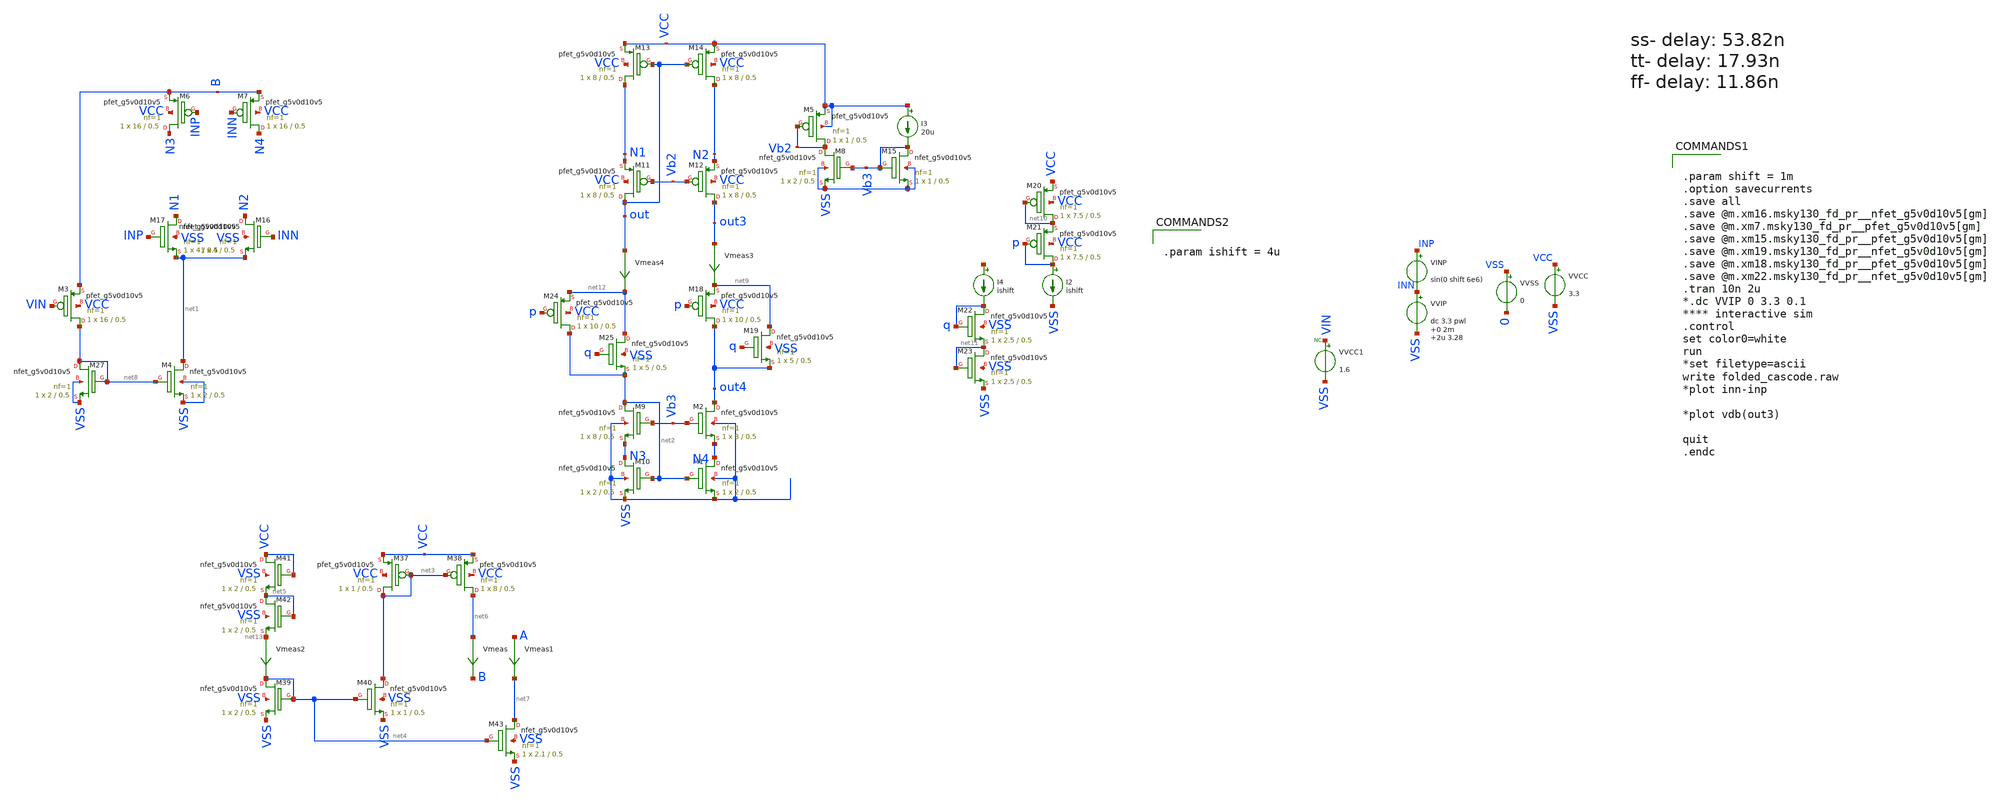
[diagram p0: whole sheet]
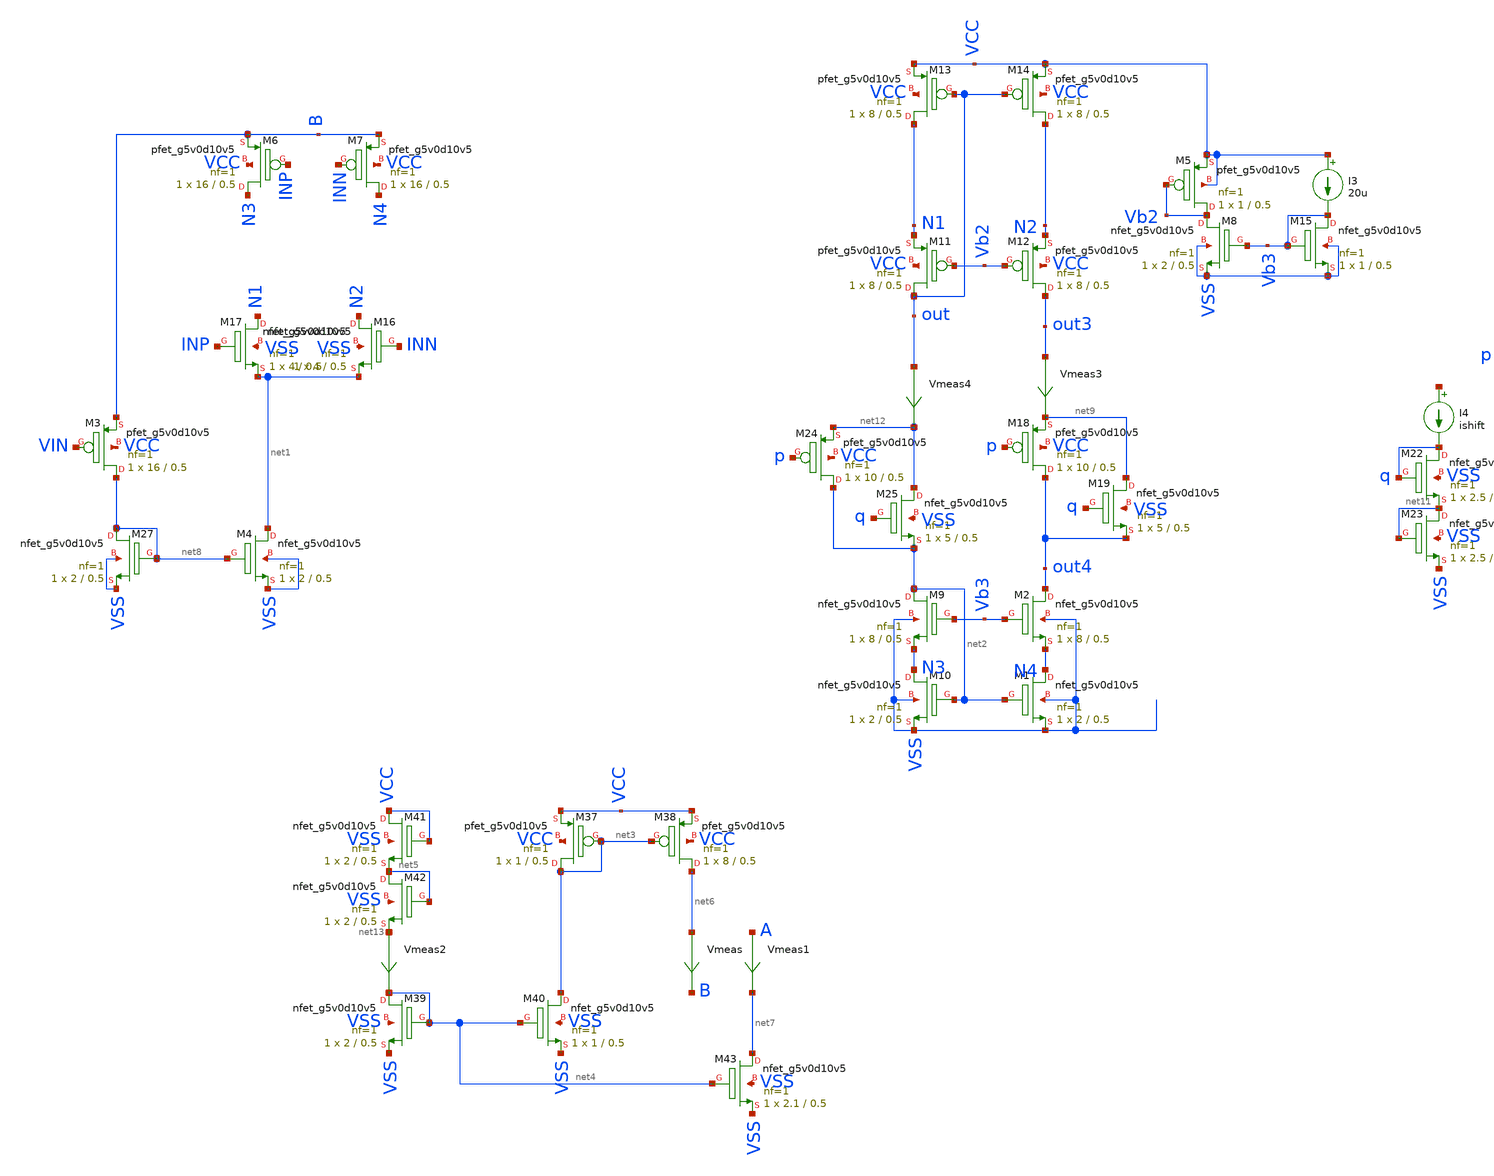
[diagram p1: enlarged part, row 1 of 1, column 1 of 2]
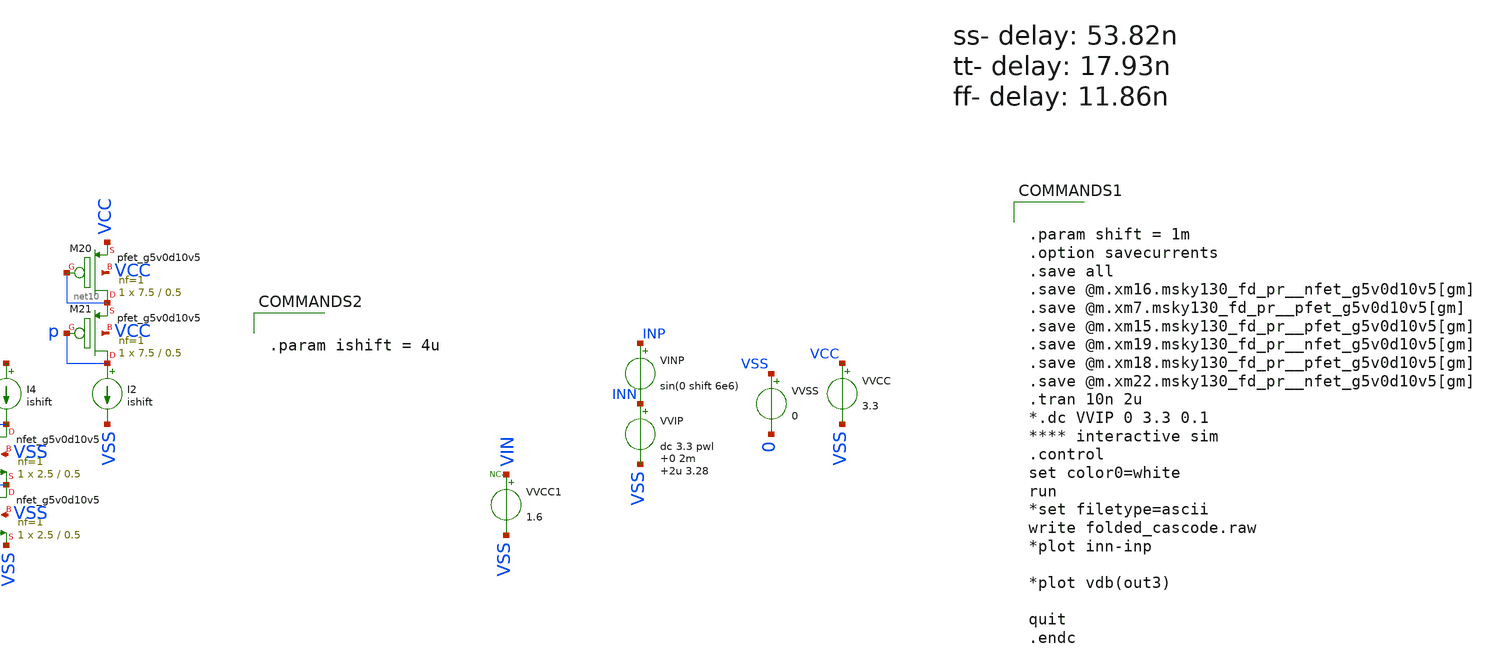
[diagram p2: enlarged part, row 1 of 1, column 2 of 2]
** sch_path: folded_cascode/folded_cascode_ab.sch
.lib $::SKYWATER_MODELS/sky130.lib.spice.tt.red tt
.include $::SKYWATER_STDCELLS/sky130_fd_sc_hd.spice

**.subckt folded_cascode_ab
XM1 N4 net2 VSS VSS sky130_fd_pr__nfet_g5v0d10v5 L=0.5 W=2 nf=1 ad='int((nf+1)/2) * W/nf * 0.29' as='int((nf+2)/2) * W/nf * 0.29'
+ pd='2*int((nf+1)/2) * (W/nf + 0.29)' ps='2*int((nf+2)/2) * (W/nf + 0.29)' nrd='0.29 / W' nrs='0.29 / W'
+ sa=0 sb=0 sd=0 mult=1 m=1
XM2 out4 Vb3 N4 VSS sky130_fd_pr__nfet_g5v0d10v5 L=0.5 W=8 nf=1 ad='int((nf+1)/2) * W/nf * 0.29' as='int((nf+2)/2) * W/nf * 0.29'
+ pd='2*int((nf+1)/2) * (W/nf + 0.29)' ps='2*int((nf+2)/2) * (W/nf + 0.29)' nrd='0.29 / W' nrs='0.29 / W'
+ sa=0 sb=0 sd=0 mult=1 m=1
XM9 net2 Vb3 N3 VSS sky130_fd_pr__nfet_g5v0d10v5 L=0.5 W=8 nf=1 ad='int((nf+1)/2) * W/nf * 0.29' as='int((nf+2)/2) * W/nf * 0.29'
+ pd='2*int((nf+1)/2) * (W/nf + 0.29)' ps='2*int((nf+2)/2) * (W/nf + 0.29)' nrd='0.29 / W' nrs='0.29 / W'
+ sa=0 sb=0 sd=0 mult=1 m=1
XM10 N3 net2 VSS VSS sky130_fd_pr__nfet_g5v0d10v5 L=0.5 W=2 nf=1 ad='int((nf+1)/2) * W/nf * 0.29' as='int((nf+2)/2) * W/nf * 0.29'
+ pd='2*int((nf+1)/2) * (W/nf + 0.29)' ps='2*int((nf+2)/2) * (W/nf + 0.29)' nrd='0.29 / W' nrs='0.29 / W'
+ sa=0 sb=0 sd=0 mult=1 m=1
XM11 out Vb2 N1 VCC sky130_fd_pr__pfet_g5v0d10v5 L=0.5 W=8 nf=1 ad='int((nf+1)/2) * W/nf * 0.29' as='int((nf+2)/2) * W/nf * 0.29'
+ pd='2*int((nf+1)/2) * (W/nf + 0.29)' ps='2*int((nf+2)/2) * (W/nf + 0.29)' nrd='0.29 / W' nrs='0.29 / W'
+ sa=0 sb=0 sd=0 mult=1 m=1
XM12 out3 Vb2 N2 VCC sky130_fd_pr__pfet_g5v0d10v5 L=0.5 W=8 nf=1 ad='int((nf+1)/2) * W/nf * 0.29' as='int((nf+2)/2) * W/nf * 0.29'
+ pd='2*int((nf+1)/2) * (W/nf + 0.29)' ps='2*int((nf+2)/2) * (W/nf + 0.29)' nrd='0.29 / W' nrs='0.29 / W'
+ sa=0 sb=0 sd=0 mult=1 m=1
XM13 N1 out VCC VCC sky130_fd_pr__pfet_g5v0d10v5 L=0.5 W=8 nf=1 ad='int((nf+1)/2) * W/nf * 0.29' as='int((nf+2)/2) * W/nf * 0.29'
+ pd='2*int((nf+1)/2) * (W/nf + 0.29)' ps='2*int((nf+2)/2) * (W/nf + 0.29)' nrd='0.29 / W' nrs='0.29 / W'
+ sa=0 sb=0 sd=0 mult=1 m=1
XM14 N2 out VCC VCC sky130_fd_pr__pfet_g5v0d10v5 L=0.5 W=8 nf=1 ad='int((nf+1)/2) * W/nf * 0.29' as='int((nf+2)/2) * W/nf * 0.29'
+ pd='2*int((nf+1)/2) * (W/nf + 0.29)' ps='2*int((nf+2)/2) * (W/nf + 0.29)' nrd='0.29 / W' nrs='0.29 / W'
+ sa=0 sb=0 sd=0 mult=1 m=1
XM16 N2 INN net1 VSS sky130_fd_pr__nfet_g5v0d10v5 L=0.5 W=4 nf=1 ad='int((nf+1)/2) * W/nf * 0.29' as='int((nf+2)/2) * W/nf * 0.29'
+ pd='2*int((nf+1)/2) * (W/nf + 0.29)' ps='2*int((nf+2)/2) * (W/nf + 0.29)' nrd='0.29 / W' nrs='0.29 / W'
+ sa=0 sb=0 sd=0 mult=1 m=1
XM17 N1 INP net1 VSS sky130_fd_pr__nfet_g5v0d10v5 L=0.5 W=4 nf=1 ad='int((nf+1)/2) * W/nf * 0.29' as='int((nf+2)/2) * W/nf * 0.29'
+ pd='2*int((nf+1)/2) * (W/nf + 0.29)' ps='2*int((nf+2)/2) * (W/nf + 0.29)' nrd='0.29 / W' nrs='0.29 / W'
+ sa=0 sb=0 sd=0 mult=1 m=1
XM6 N3 INP B VCC sky130_fd_pr__pfet_g5v0d10v5 L=0.5 W=16 nf=1 ad='int((nf+1)/2) * W/nf * 0.29' as='int((nf+2)/2) * W/nf * 0.29'
+ pd='2*int((nf+1)/2) * (W/nf + 0.29)' ps='2*int((nf+2)/2) * (W/nf + 0.29)' nrd='0.29 / W' nrs='0.29 / W'
+ sa=0 sb=0 sd=0 mult=1 m=1
XM7 N4 INN B VCC sky130_fd_pr__pfet_g5v0d10v5 L=0.5 W=16 nf=1 ad='int((nf+1)/2) * W/nf * 0.29' as='int((nf+2)/2) * W/nf * 0.29'
+ pd='2*int((nf+1)/2) * (W/nf + 0.29)' ps='2*int((nf+2)/2) * (W/nf + 0.29)' nrd='0.29 / W' nrs='0.29 / W'
+ sa=0 sb=0 sd=0 mult=1 m=1
XM37 net3 net3 VCC VCC sky130_fd_pr__pfet_g5v0d10v5 L=0.5 W=1 nf=1 ad='int((nf+1)/2) * W/nf * 0.29' as='int((nf+2)/2) * W/nf * 0.29'
+ pd='2*int((nf+1)/2) * (W/nf + 0.29)' ps='2*int((nf+2)/2) * (W/nf + 0.29)' nrd='0.29 / W' nrs='0.29 / W'
+ sa=0 sb=0 sd=0 mult=1 m=1
XM38 net6 net3 VCC VCC sky130_fd_pr__pfet_g5v0d10v5 L=0.5 W=8 nf=1 ad='int((nf+1)/2) * W/nf * 0.29' as='int((nf+2)/2) * W/nf * 0.29'
+ pd='2*int((nf+1)/2) * (W/nf + 0.29)' ps='2*int((nf+2)/2) * (W/nf + 0.29)' nrd='0.29 / W' nrs='0.29 / W'
+ sa=0 sb=0 sd=0 mult=1 m=1
Vmeas net6 B 0
.save i(vmeas)
XM39 net4 net4 VSS VSS sky130_fd_pr__nfet_g5v0d10v5 L=0.5 W=2 nf=1 ad='int((nf+1)/2) * W/nf * 0.29' as='int((nf+2)/2) * W/nf * 0.29'
+ pd='2*int((nf+1)/2) * (W/nf + 0.29)' ps='2*int((nf+2)/2) * (W/nf + 0.29)' nrd='0.29 / W' nrs='0.29 / W'
+ sa=0 sb=0 sd=0 mult=1 m=1
XM40 net3 net4 VSS VSS sky130_fd_pr__nfet_g5v0d10v5 L=0.5 W=1 nf=1 ad='int((nf+1)/2) * W/nf * 0.29' as='int((nf+2)/2) * W/nf * 0.29'
+ pd='2*int((nf+1)/2) * (W/nf + 0.29)' ps='2*int((nf+2)/2) * (W/nf + 0.29)' nrd='0.29 / W' nrs='0.29 / W'
+ sa=0 sb=0 sd=0 mult=1 m=1
Vmeas2 net13 net4 0
.save i(vmeas2)
XM41 VCC VCC net5 VSS sky130_fd_pr__nfet_g5v0d10v5 L=0.5 W=2 nf=1 ad='int((nf+1)/2) * W/nf * 0.29' as='int((nf+2)/2) * W/nf * 0.29'
+ pd='2*int((nf+1)/2) * (W/nf + 0.29)' ps='2*int((nf+2)/2) * (W/nf + 0.29)' nrd='0.29 / W' nrs='0.29 / W'
+ sa=0 sb=0 sd=0 mult=1 m=1
XM42 net5 net5 net13 VSS sky130_fd_pr__nfet_g5v0d10v5 L=0.5 W=2 nf=1 ad='int((nf+1)/2) * W/nf * 0.29'
+ as='int((nf+2)/2) * W/nf * 0.29' pd='2*int((nf+1)/2) * (W/nf + 0.29)' ps='2*int((nf+2)/2) * (W/nf + 0.29)'
+ nrd='0.29 / W' nrs='0.29 / W' sa=0 sb=0 sd=0 mult=1 m=1
XM43 net7 net4 VSS VSS sky130_fd_pr__nfet_g5v0d10v5 L=0.5 W=2.1 nf=1 ad='int((nf+1)/2) * W/nf * 0.29'
+ as='int((nf+2)/2) * W/nf * 0.29' pd='2*int((nf+1)/2) * (W/nf + 0.29)' ps='2*int((nf+2)/2) * (W/nf + 0.29)'
+ nrd='0.29 / W' nrs='0.29 / W' sa=0 sb=0 sd=0 mult=1 m=1
Vmeas1 A net7 0
.save i(vmeas1)
VINP INP INN sin(0 shift 6e6)
VVSS VSS 0 0
VVCC VCC VSS 3.3
VVIP INN VSS dc 3.3 pwl 0 2m 2u 3.28

VVCC1 VIN VSS 1.6
* noconn VIN
XM4 net1 net8 VSS VSS sky130_fd_pr__nfet_g5v0d10v5 L=0.5 W=2 nf=1 ad='int((nf+1)/2) * W/nf * 0.29' as='int((nf+2)/2) * W/nf * 0.29'
+ pd='2*int((nf+1)/2) * (W/nf + 0.29)' ps='2*int((nf+2)/2) * (W/nf + 0.29)' nrd='0.29 / W' nrs='0.29 / W'
+ sa=0 sb=0 sd=0 mult=1 m=1
XM27 net8 net8 VSS VSS sky130_fd_pr__nfet_g5v0d10v5 L=0.5 W=2 nf=1 ad='int((nf+1)/2) * W/nf * 0.29' as='int((nf+2)/2) * W/nf * 0.29'
+ pd='2*int((nf+1)/2) * (W/nf + 0.29)' ps='2*int((nf+2)/2) * (W/nf + 0.29)' nrd='0.29 / W' nrs='0.29 / W'
+ sa=0 sb=0 sd=0 mult=1 m=1
XM3 net8 VIN B VCC sky130_fd_pr__pfet_g5v0d10v5 L=0.5 W=16 nf=1 ad='int((nf+1)/2) * W/nf * 0.29' as='int((nf+2)/2) * W/nf * 0.29'
+ pd='2*int((nf+1)/2) * (W/nf + 0.29)' ps='2*int((nf+2)/2) * (W/nf + 0.29)' nrd='0.29 / W' nrs='0.29 / W'
+ sa=0 sb=0 sd=0 mult=1 m=1
XM5 Vb2 Vb2 VCC VCC sky130_fd_pr__pfet_g5v0d10v5 L=0.5 W=1 nf=1 ad='int((nf+1)/2) * W/nf * 0.29' as='int((nf+2)/2) * W/nf * 0.29'
+ pd='2*int((nf+1)/2) * (W/nf + 0.29)' ps='2*int((nf+2)/2) * (W/nf + 0.29)' nrd='0.29 / W' nrs='0.29 / W'
+ sa=0 sb=0 sd=0 mult=1 m=1
XM8 Vb2 Vb3 VSS VSS sky130_fd_pr__nfet_g5v0d10v5 L=0.5 W=2 nf=1 ad='int((nf+1)/2) * W/nf * 0.29' as='int((nf+2)/2) * W/nf * 0.29'
+ pd='2*int((nf+1)/2) * (W/nf + 0.29)' ps='2*int((nf+2)/2) * (W/nf + 0.29)' nrd='0.29 / W' nrs='0.29 / W'
+ sa=0 sb=0 sd=0 mult=1 m=1
XM15 Vb3 Vb3 VSS VSS sky130_fd_pr__nfet_g5v0d10v5 L=0.5 W=1 nf=1 ad='int((nf+1)/2) * W/nf * 0.29' as='int((nf+2)/2) * W/nf * 0.29'
+ pd='2*int((nf+1)/2) * (W/nf + 0.29)' ps='2*int((nf+2)/2) * (W/nf + 0.29)' nrd='0.29 / W' nrs='0.29 / W'
+ sa=0 sb=0 sd=0 mult=1 m=1
I3 VCC Vb3 20u
XM18 out4 p net9 VCC sky130_fd_pr__pfet_g5v0d10v5 L=0.5 W=10 nf=1 ad='int((nf+1)/2) * W/nf * 0.29' as='int((nf+2)/2) * W/nf * 0.29'
+ pd='2*int((nf+1)/2) * (W/nf + 0.29)' ps='2*int((nf+2)/2) * (W/nf + 0.29)' nrd='0.29 / W' nrs='0.29 / W'
+ sa=0 sb=0 sd=0 mult=1 m=1
XM19 net9 q out4 VSS sky130_fd_pr__nfet_g5v0d10v5 L=0.5 W=5 nf=1 ad='int((nf+1)/2) * W/nf * 0.29' as='int((nf+2)/2) * W/nf * 0.29'
+ pd='2*int((nf+1)/2) * (W/nf + 0.29)' ps='2*int((nf+2)/2) * (W/nf + 0.29)' nrd='0.29 / W' nrs='0.29 / W'
+ sa=0 sb=0 sd=0 mult=1 m=1
Vmeas3 out3 net9 0
.save i(vmeas3)
Vmeas4 out net12 0
.save i(vmeas4)
XM20 net10 net10 VCC VCC sky130_fd_pr__pfet_g5v0d10v5 L=0.5 W=7.5 nf=1 ad='int((nf+1)/2) * W/nf * 0.29'
+ as='int((nf+2)/2) * W/nf * 0.29' pd='2*int((nf+1)/2) * (W/nf + 0.29)' ps='2*int((nf+2)/2) * (W/nf + 0.29)'
+ nrd='0.29 / W' nrs='0.29 / W' sa=0 sb=0 sd=0 mult=1 m=1
XM21 p p net10 VCC sky130_fd_pr__pfet_g5v0d10v5 L=0.5 W=7.5 nf=1 ad='int((nf+1)/2) * W/nf * 0.29' as='int((nf+2)/2) * W/nf * 0.29'
+ pd='2*int((nf+1)/2) * (W/nf + 0.29)' ps='2*int((nf+2)/2) * (W/nf + 0.29)' nrd='0.29 / W' nrs='0.29 / W'
+ sa=0 sb=0 sd=0 mult=1 m=1
XM22 q q net11 VSS sky130_fd_pr__nfet_g5v0d10v5 L=0.5 W=2.5 nf=1 ad='int((nf+1)/2) * W/nf * 0.29' as='int((nf+2)/2) * W/nf * 0.29'
+ pd='2*int((nf+1)/2) * (W/nf + 0.29)' ps='2*int((nf+2)/2) * (W/nf + 0.29)' nrd='0.29 / W' nrs='0.29 / W'
+ sa=0 sb=0 sd=0 mult=1 m=1
I2 p VSS ishift
XM23 net11 net11 VSS VSS sky130_fd_pr__nfet_g5v0d10v5 L=0.5 W=2.5 nf=1 ad='int((nf+1)/2) * W/nf * 0.29'
+ as='int((nf+2)/2) * W/nf * 0.29' pd='2*int((nf+1)/2) * (W/nf + 0.29)' ps='2*int((nf+2)/2) * (W/nf + 0.29)'
+ nrd='0.29 / W' nrs='0.29 / W' sa=0 sb=0 sd=0 mult=1 m=1
I4 net14 q ishift
XM24 net2 p net12 VCC sky130_fd_pr__pfet_g5v0d10v5 L=0.5 W=10 nf=1 ad='int((nf+1)/2) * W/nf * 0.29' as='int((nf+2)/2) * W/nf * 0.29'
+ pd='2*int((nf+1)/2) * (W/nf + 0.29)' ps='2*int((nf+2)/2) * (W/nf + 0.29)' nrd='0.29 / W' nrs='0.29 / W'
+ sa=0 sb=0 sd=0 mult=1 m=1
XM25 net12 q net2 VSS sky130_fd_pr__nfet_g5v0d10v5 L=0.5 W=5 nf=1 ad='int((nf+1)/2) * W/nf * 0.29' as='int((nf+2)/2) * W/nf * 0.29'
+ pd='2*int((nf+1)/2) * (W/nf + 0.29)' ps='2*int((nf+2)/2) * (W/nf + 0.29)' nrd='0.29 / W' nrs='0.29 / W'
+ sa=0 sb=0 sd=0 mult=1 m=1
**** begin user architecture code


.param shift = 1m
.option savecurrents
.save all
.save @m.xm16.msky130_fd_pr__nfet_g5v0d10v5[gm]
.save @m.xm7.msky130_fd_pr__pfet_g5v0d10v5[gm]
.save @m.xm15.msky130_fd_pr__pfet_g5v0d10v5[gm]
.save @m.xm19.msky130_fd_pr__nfet_g5v0d10v5[gm]
.save @m.xm18.msky130_fd_pr__pfet_g5v0d10v5[gm]
.save @m.xm22.msky130_fd_pr__nfet_g5v0d10v5[gm]
.tran 10n 2u
*.dc VVIP 0 3.3 0.1
**** interactive sim
.control
set color0=white
run
*set filetype=ascii
write folded_cascode.raw
*plot inn-inp

*plot vdb(out3)

quit
.endc




.param ishift = 4u


**** end user architecture code
**.ends
.end
